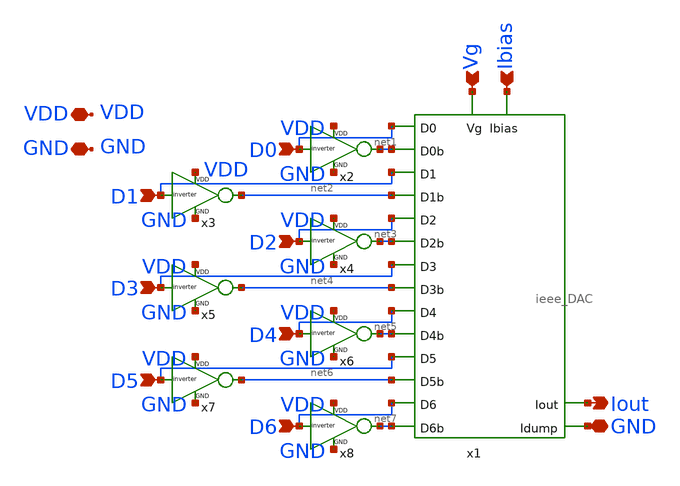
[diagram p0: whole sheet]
** sch_path: schematics/ieee_simple_M_2M_DAC.sch
**.subckt ieee_simple_M_2M_DAC GND Ibias Iout D0 D1 D2 D3 D4 D5 D6 Vg VDD GND
*.iopin GND
*.ipin Ibias
*.opin Iout
*.ipin D0
*.ipin D1
*.ipin D2
*.ipin D3
*.ipin D4
*.ipin D5
*.ipin D6
*.ipin Vg
*.iopin VDD
*.iopin GND
x1 Ibias Vg D0 D2 D3 D4 D5 net6 D1 net1 net2 net3 net4 net5 D6 net7 Iout GND ieee_DAC
x2 VDD D0 net1 GND inverter
x3 VDD D1 net2 GND inverter
x4 VDD D2 net3 GND inverter
x5 VDD D3 net4 GND inverter
x6 VDD D4 net5 GND inverter
x7 VDD D5 net6 GND inverter
x8 VDD D6 net7 GND inverter
**.ends
.end
